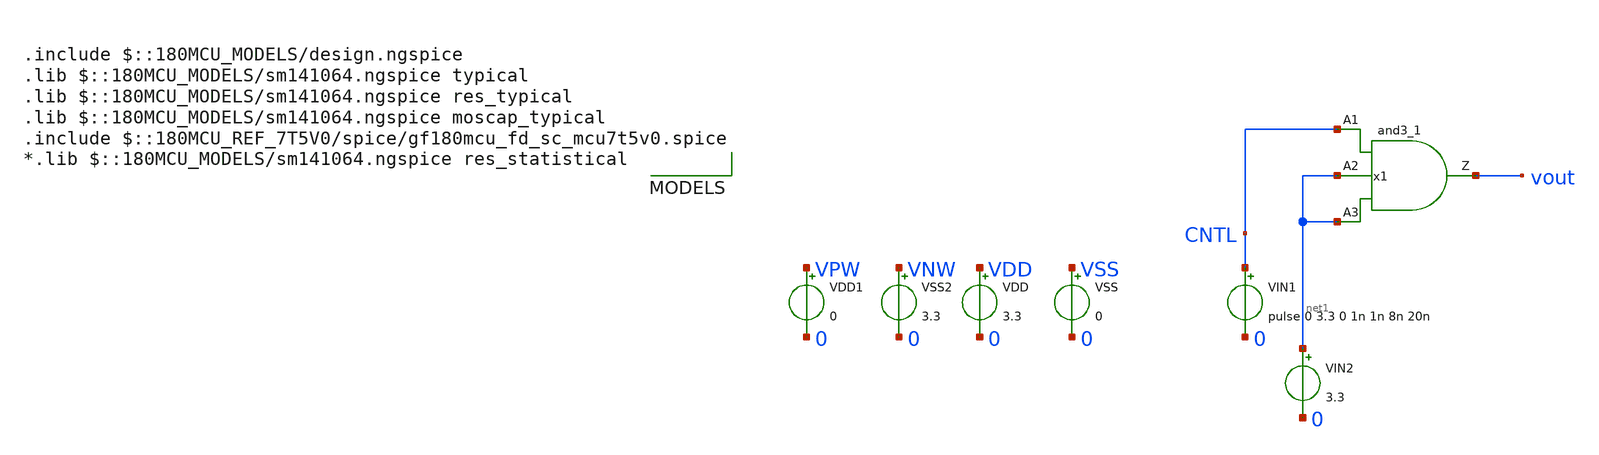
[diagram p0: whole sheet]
** sch_path: DAC/xschem/std_cell/tb_fiiles/Test_and3.sch
**.subckt Test_and3
VIN1 CNTL 0 pulse 0 3.3 0 1n 1n 8n 20n
VIN2 net1 0 3.3
VDD VDD 0 3.3
VSS VSS 0 0
VDD1 VPW 0 0
VSS2 VNW 0 3.3
x1 CNTL net1 net1 vout VDD VNW VPW VSS gf180mcu_fd_sc_mcu7t5v0__and3_1
**** begin user architecture code

.include $::180MCU_MODELS/design.ngspice
.lib $::180MCU_MODELS/sm141064.ngspice typical
.lib $::180MCU_MODELS/sm141064.ngspice res_typical
.lib $::180MCU_MODELS/sm141064.ngspice moscap_typical
.include $::180MCU_REF_7T5V0/spice/gf180mcu_fd_sc_mcu7t5v0.spice
*.lib $::180MCU_MODELS/sm141064.ngspice res_statistical





.control
	tran 0.1n 50n
	*dc vin1 0 3.3 0.1
	plot v(CNTL) V(vout)
	plot v(vout)
	write test_and.raw

.endc
.save all




**** end user architecture code
**.ends
.end
